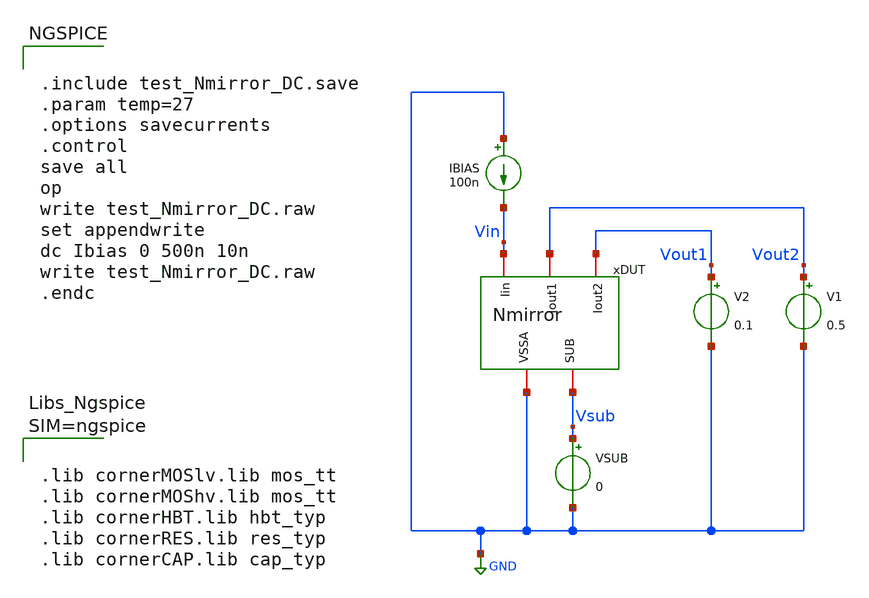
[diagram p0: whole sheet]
** sch_path: xschem/test_Nmirror_DC.sch
**.subckt test_Nmirror_DC
xDUT Vout1 Vin Vout2 GND Vsub Nmirror
IBIAS GND Vin 100n
V1 Vout2 GND 0.5
.save i(v1)
V2 Vout1 GND 0.1
.save i(v2)
VSUB Vsub GND 0
.save i(vsub)
**** begin user architecture code


.include test_Nmirror_DC.save
.param temp=27
.options savecurrents
.control
save all
op
write test_Nmirror_DC.raw
set appendwrite
dc Ibias 0 500n 10n
write test_Nmirror_DC.raw
.endc





.lib cornerMOSlv.lib mos_tt
.lib cornerMOShv.lib mos_tt
.lib cornerHBT.lib hbt_typ
.lib cornerRES.lib res_typ
.lib cornerCAP.lib cap_typ



**** end user architecture code
**.ends

* expanding   symbol:  Nmirror.sym # of pins=5
** sym_path: Nmirror.sym
** sch_path: Nmirror.sch
.subckt Nmirror Iout2 Iin Iout1 VSSA SUB
*.iopin VSSA
*.iopin SUB
*.iopin Iin
*.iopin Iout1
*.iopin Iout2
XM1 net3 Iin VSSA SUB sg13_lv_nmos w=1.0u l=4.0u ng=1 m=1 mm_ok=1
XM3 net2 Iin VSSA SUB sg13_lv_nmos w=1.0u l=4.0u ng=1 m=1 mm_ok=1
XM2 Iin Iin net3 SUB sg13_lv_nmos w=1.0u l=0.26u ng=1 m=1 mm_ok=1
XM4 Iout1 Iin net2 SUB sg13_lv_nmos w=1.0u l=0.26u ng=1 m=1 mm_ok=1
XM5 net1 Iin VSSA SUB sg13_lv_nmos w=1.0u l=4.0u ng=1 m=1 mm_ok=1
XM6 Iout2 Iin net1 SUB sg13_lv_nmos w=1.0u l=0.26u ng=1 m=1 mm_ok=1
.ends

.GLOBAL GND
.end
